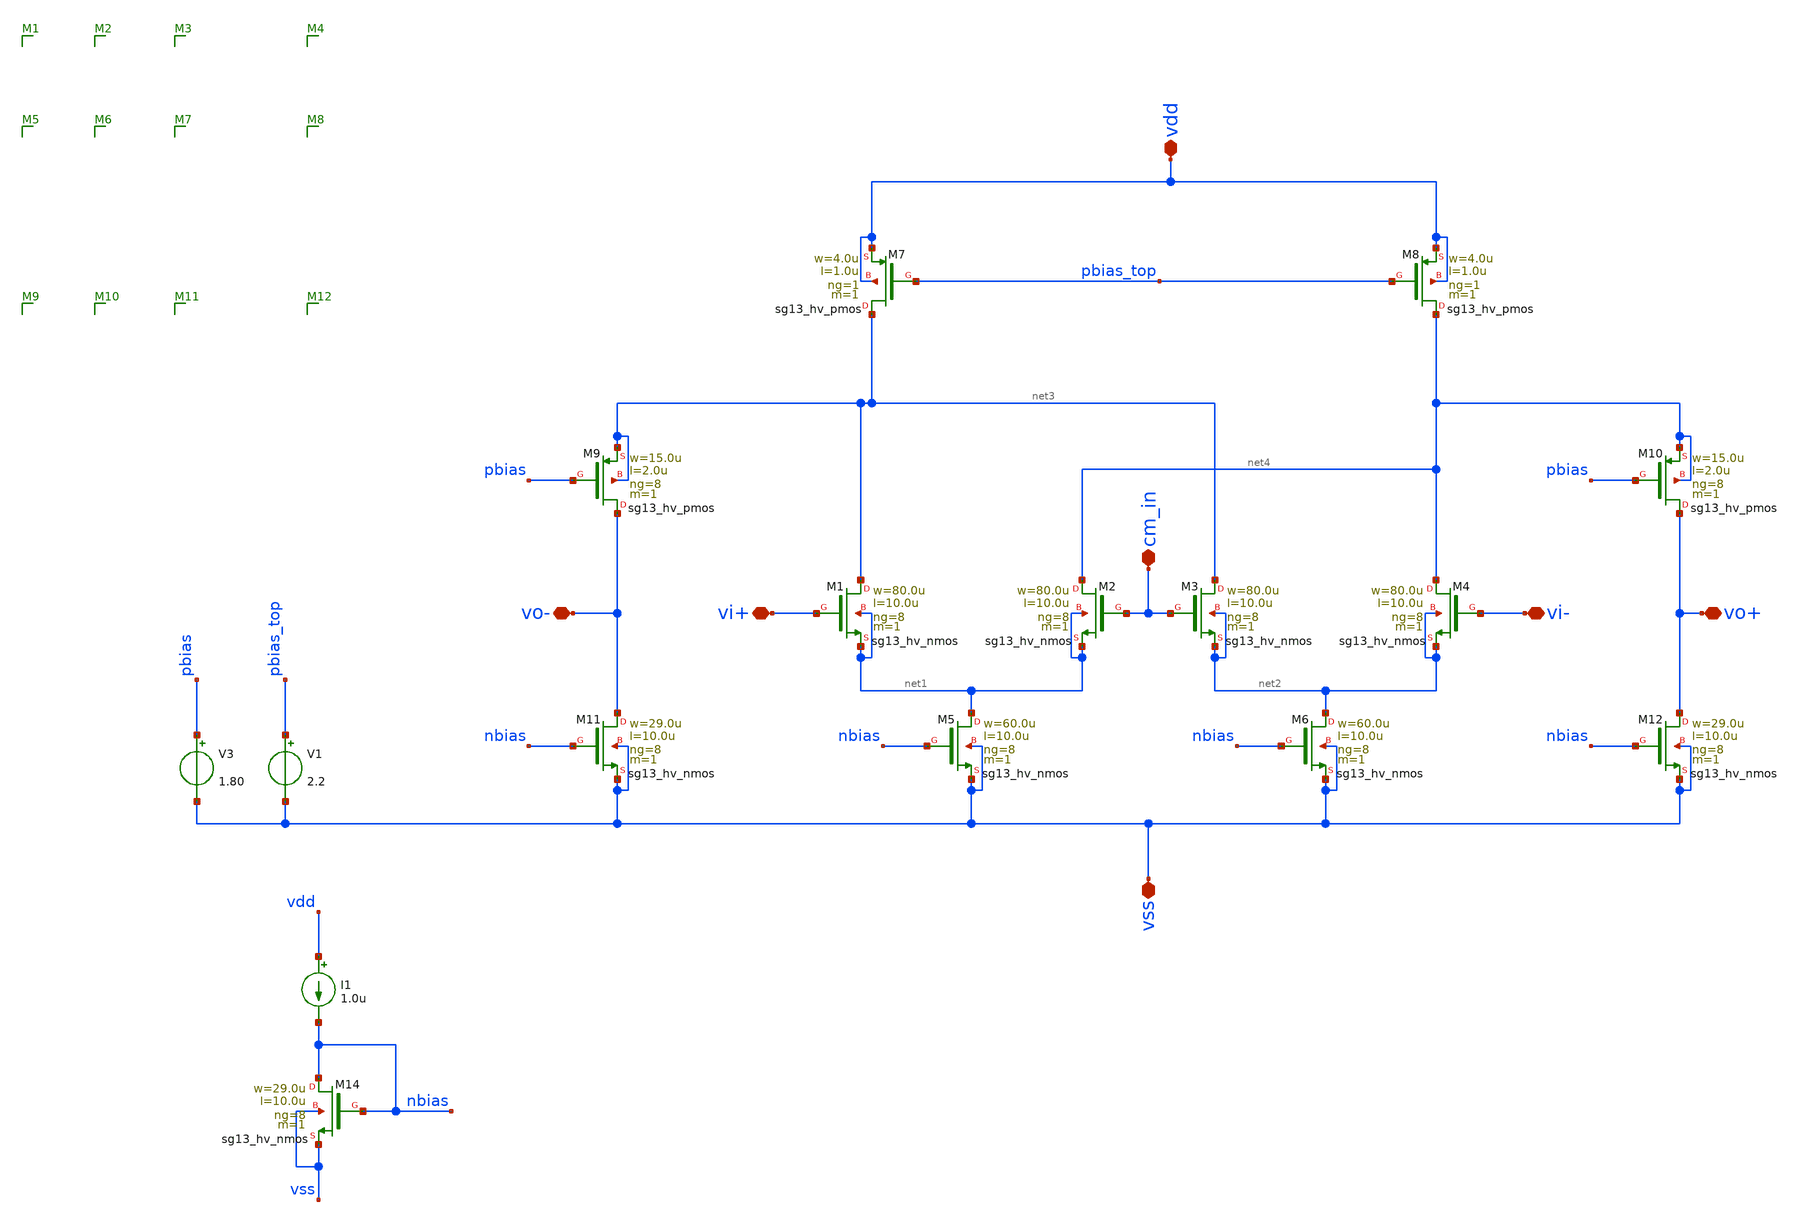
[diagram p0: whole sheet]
** sch_path: schematic/aux_amp.sch
**.subckt aux_amp vss vo- vdd vo+ vi- vi+ cm_in
*.iopin vss
*.iopin vo-
*.iopin vdd
*.iopin vo+
*.iopin vi-
*.iopin vi+
*.iopin cm_in
XM1 net3 vi+ net1 net1 sg13_hv_nmos w=80.0u l=10.0u ng=8 m=1 mm_ok=1
XM2 net4 cm_in net1 net1 sg13_hv_nmos w=80.0u l=10.0u ng=8 m=1 mm_ok=1
XM5 net1 nbias vss vss sg13_hv_nmos w=60.0u l=10.0u ng=8 m=1 mm_ok=1
XM3 net3 cm_in net2 net2 sg13_hv_nmos w=80.0u l=10.0u ng=8 m=1 mm_ok=1
XM4 net4 vi- net2 net2 sg13_hv_nmos w=80.0u l=10.0u ng=8 m=1 mm_ok=1
XM6 net2 nbias vss vss sg13_hv_nmos w=60.0u l=10.0u ng=8 m=1 mm_ok=1
XM11 vo- nbias vss vss sg13_hv_nmos w=29.0u l=10.0u ng=8 m=1 mm_ok=1
XM12 vo+ nbias vss vss sg13_hv_nmos w=29.0u l=10.0u ng=8 m=1 mm_ok=1
V3 pbias vss 1.80
XM9 vo- pbias net3 net3 sg13_hv_pmos w=15.0u l=2.0u ng=8 m=1 mm_ok=1
XM7 net3 pbias_top vdd vdd sg13_hv_pmos w=4.0u l=1.0u ng=1 m=1 mm_ok=1
XM8 net4 pbias_top vdd vdd sg13_hv_pmos w=4.0u l=1.0u ng=1 m=1 mm_ok=1
XM10 vo+ pbias net4 net4 sg13_hv_pmos w=15.0u l=2.0u ng=8 m=1 mm_ok=1
XM14 nbias nbias vss vss sg13_hv_nmos w=29.0u l=10.0u ng=8 m=1 mm_ok=1
I1 vdd nbias 1.0u
V1 pbias_top vss 2.2
**.ends
.end
